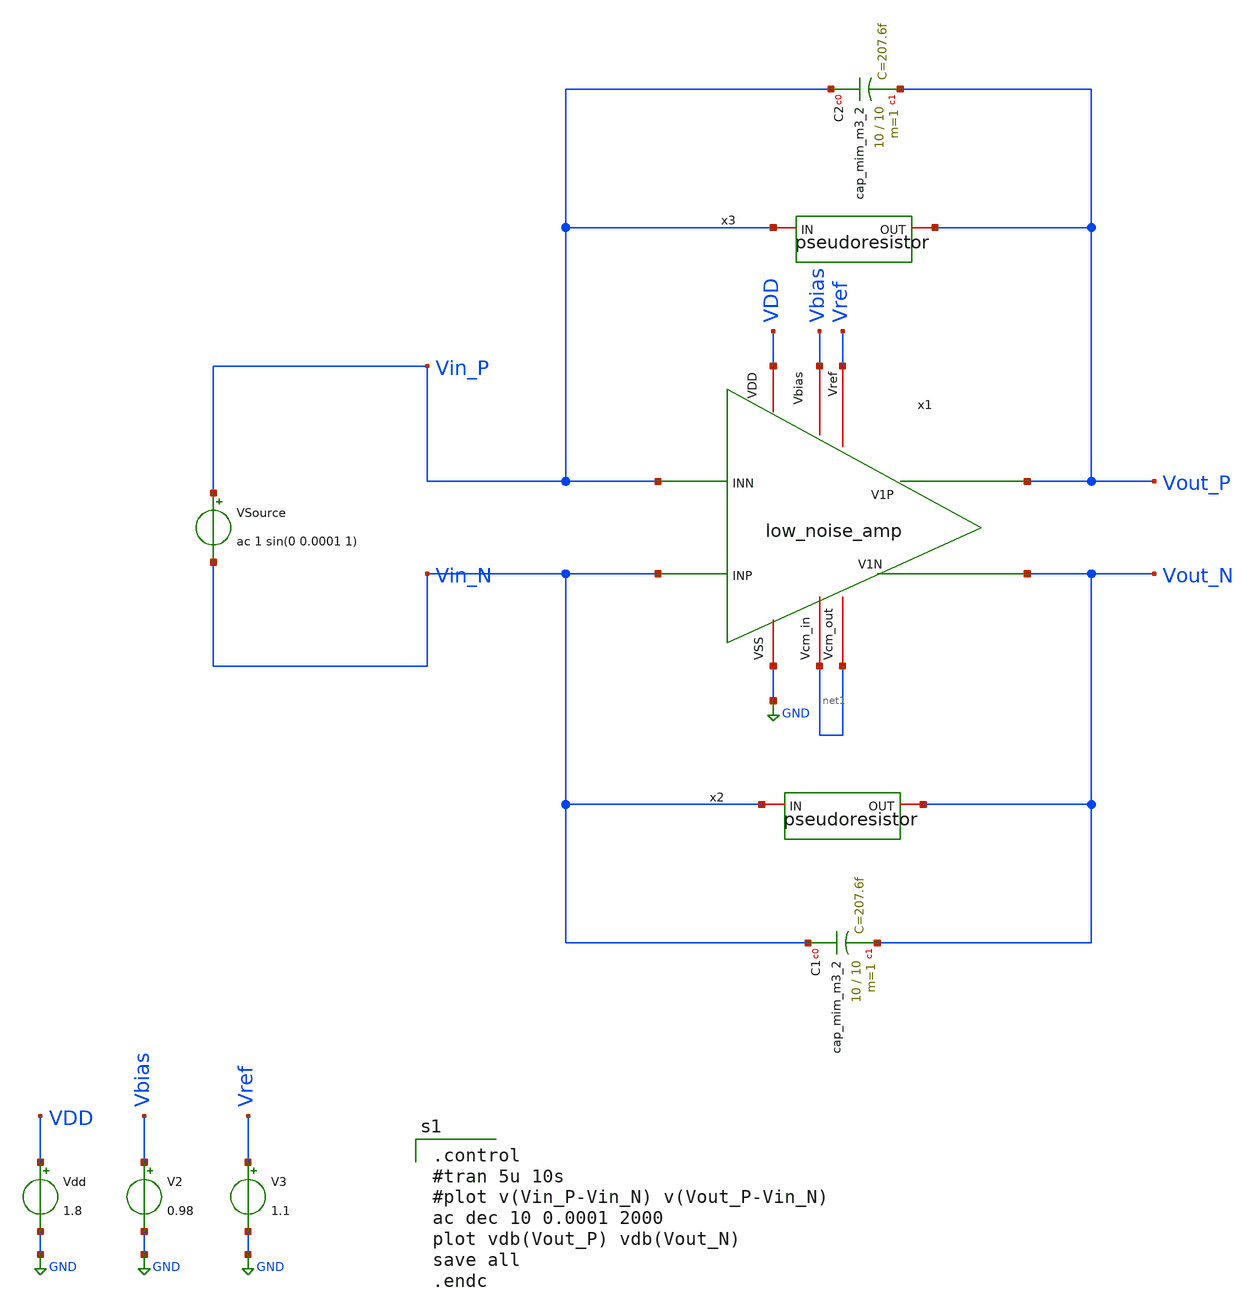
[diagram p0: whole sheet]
** sch_path: opamp_lna/low_noise_amp_tb.sch
**.subckt low_noise_amp_tb
x1 VDD net1 Vin_P Vin_N Vout_P Vout_N GND net1 Vbias Vref low_noise_amp
Vdd VDD GND 1.8
V2 Vbias GND 0.98
V3 Vref GND 1.1
VSource Vin_P Vin_N ac 1 sin(0 0.0001 1)
x2 Vin_N Vout_N pseudoresistor
x3 Vin_P Vout_P pseudoresistor
XC1 Vin_N Vout_N sky130_fd_pr__cap_mim_m3_2 W=10 L=10 MF=1 m=1
XC2 Vin_P Vout_P sky130_fd_pr__cap_mim_m3_2 W=10 L=10 MF=1 m=1
**** begin user architecture code

** opencircuitdesign pdks install
.lib $::SKYWATER_MODELS/sky130.lib.spice tt



.control
#tran 5u 10s
#plot v(Vin_P-Vin_N) v(Vout_P-Vin_N)
ac dec 10 0.0001 2000
plot vdb(Vout_P) vdb(Vout_N)
save all
.endc

**** end user architecture code
**.ends

* expanding   symbol:  low_noise_amp.sym # of pins=10
** sym_path: opamp_lna/low_noise_amp.sym
** sch_path: opamp_lna/low_noise_amp.sch
.subckt low_noise_amp VDD Vcm_in INN INP V1P V1N VSS Vcm_out Vbias Vref
*.iopin VDD
*.iopin VSS
*.iopin Vbias
*.ipin INP
*.ipin INN
*.iopin Vref
*.iopin Vcm_in
*.iopin Vcm_out
*.opin V1N
*.opin V1P
XM3 CMFB Vref net1 VDD sky130_fd_pr__pfet_01v8 L=0.8 W=4 nf=1 ad='int((nf+1)/2) * W/nf * 0.29' as='int((nf+2)/2) * W/nf * 0.29'
+ pd='2*int((nf+1)/2) * (W/nf + 0.29)' ps='2*int((nf+2)/2) * (W/nf + 0.29)' nrd='0.29 / W' nrs='0.29 / W'
+ sa=0 sb=0 sd=0 mult=1 m=1
XM11 net1 Vbias VDD VDD sky130_fd_pr__pfet_01v8 L=0.8 W=1 nf=1 ad='int((nf+1)/2) * W/nf * 0.29' as='int((nf+2)/2) * W/nf * 0.29'
+ pd='2*int((nf+1)/2) * (W/nf + 0.29)' ps='2*int((nf+2)/2) * (W/nf + 0.29)' nrd='0.29 / W' nrs='0.29 / W'
+ sa=0 sb=0 sd=0 mult=1 m=1
XM7 V1N INP B0 VDD sky130_fd_pr__pfet_01v8 L=2 W=16 nf=1 ad='int((nf+1)/2) * W/nf * 0.29' as='int((nf+2)/2) * W/nf * 0.29'
+ pd='2*int((nf+1)/2) * (W/nf + 0.29)' ps='2*int((nf+2)/2) * (W/nf + 0.29)' nrd='0.29 / W' nrs='0.29 / W'
+ sa=0 sb=0 sd=0 mult=1 m=1
XM8 V1P INN B0 VDD sky130_fd_pr__pfet_01v8 L=2 W=16 nf=1 ad='int((nf+1)/2) * W/nf * 0.29' as='int((nf+2)/2) * W/nf * 0.29'
+ pd='2*int((nf+1)/2) * (W/nf + 0.29)' ps='2*int((nf+2)/2) * (W/nf + 0.29)' nrd='0.29 / W' nrs='0.29 / W'
+ sa=0 sb=0 sd=0 mult=1 m=1
XM9 V1N INP net3 VSS sky130_fd_pr__nfet_01v8 L=1 W=8 nf=1 ad='int((nf+1)/2) * W/nf * 0.29' as='int((nf+2)/2) * W/nf * 0.29'
+ pd='2*int((nf+1)/2) * (W/nf + 0.29)' ps='2*int((nf+2)/2) * (W/nf + 0.29)' nrd='0.29 / W' nrs='0.29 / W'
+ sa=0 sb=0 sd=0 mult=1 m=1
XM12 B0 Vbias VDD VDD sky130_fd_pr__pfet_01v8 L=0.800 W=2 nf=1 ad='int((nf+1)/2) * W/nf * 0.29' as='int((nf+2)/2) * W/nf * 0.29'
+ pd='2*int((nf+1)/2) * (W/nf + 0.29)' ps='2*int((nf+2)/2) * (W/nf + 0.29)' nrd='0.29 / W' nrs='0.29 / W'
+ sa=0 sb=0 sd=0 mult=1 m=1
XM13 net3 CMFB VSS VSS sky130_fd_pr__nfet_01v8 L=0.8 W=2 nf=1 ad='int((nf+1)/2) * W/nf * 0.29' as='int((nf+2)/2) * W/nf * 0.29'
+ pd='2*int((nf+1)/2) * (W/nf + 0.29)' ps='2*int((nf+2)/2) * (W/nf + 0.29)' nrd='0.29 / W' nrs='0.29 / W'
+ sa=0 sb=0 sd=0 mult=1 m=1
XM15 Vcm_out Vcm_out net4 Vcm_out sky130_fd_pr__pfet_01v8 L=0.15 W=1 nf=1 ad='int((nf+1)/2) * W/nf * 0.29'
+ as='int((nf+2)/2) * W/nf * 0.29' pd='2*int((nf+1)/2) * (W/nf + 0.29)' ps='2*int((nf+2)/2) * (W/nf + 0.29)'
+ nrd='0.29 / W' nrs='0.29 / W' sa=0 sb=0 sd=0 mult=1 m=1
XM16 net4 V1P V1P V1P sky130_fd_pr__pfet_01v8 L=0.15 W=1 nf=1 ad='int((nf+1)/2) * W/nf * 0.29' as='int((nf+2)/2) * W/nf * 0.29'
+ pd='2*int((nf+1)/2) * (W/nf + 0.29)' ps='2*int((nf+2)/2) * (W/nf + 0.29)' nrd='0.29 / W' nrs='0.29 / W'
+ sa=0 sb=0 sd=0 mult=1 m=1
XM17 Vcm_out Vcm_out net5 Vcm_out sky130_fd_pr__pfet_01v8 L=0.15 W=1 nf=1 ad='int((nf+1)/2) * W/nf * 0.29'
+ as='int((nf+2)/2) * W/nf * 0.29' pd='2*int((nf+1)/2) * (W/nf + 0.29)' ps='2*int((nf+2)/2) * (W/nf + 0.29)'
+ nrd='0.29 / W' nrs='0.29 / W' sa=0 sb=0 sd=0 mult=1 m=1
XM18 net5 V1N V1N V1N sky130_fd_pr__pfet_01v8 L=0.15 W=1 nf=1 ad='int((nf+1)/2) * W/nf * 0.29' as='int((nf+2)/2) * W/nf * 0.29'
+ pd='2*int((nf+1)/2) * (W/nf + 0.29)' ps='2*int((nf+2)/2) * (W/nf + 0.29)' nrd='0.29 / W' nrs='0.29 / W'
+ sa=0 sb=0 sd=0 mult=1 m=1
XC1 Vcm_out VSS sky130_fd_pr__cap_mim_m3_1 W=1 L=1 MF=1 m=1
XM1 V1P INN net3 VSS sky130_fd_pr__nfet_01v8 L=1 W=8 nf=1 ad='int((nf+1)/2) * W/nf * 0.29' as='int((nf+2)/2) * W/nf * 0.29'
+ pd='2*int((nf+1)/2) * (W/nf + 0.29)' ps='2*int((nf+2)/2) * (W/nf + 0.29)' nrd='0.29 / W' nrs='0.29 / W'
+ sa=0 sb=0 sd=0 mult=1 m=1
XM2 net2 net2 VSS VSS sky130_fd_pr__nfet_01v8 L=0.8 W=2 nf=1 ad='int((nf+1)/2) * W/nf * 0.29' as='int((nf+2)/2) * W/nf * 0.29'
+ pd='2*int((nf+1)/2) * (W/nf + 0.29)' ps='2*int((nf+2)/2) * (W/nf + 0.29)' nrd='0.29 / W' nrs='0.29 / W'
+ sa=0 sb=0 sd=0 mult=1 m=1
XM5 CMFB net2 VSS VSS sky130_fd_pr__nfet_01v8 L=0.8 W=2 nf=1 ad='int((nf+1)/2) * W/nf * 0.29' as='int((nf+2)/2) * W/nf * 0.29'
+ pd='2*int((nf+1)/2) * (W/nf + 0.29)' ps='2*int((nf+2)/2) * (W/nf + 0.29)' nrd='0.29 / W' nrs='0.29 / W'
+ sa=0 sb=0 sd=0 mult=1 m=1
XM6 net2 Vcm_in net1 VDD sky130_fd_pr__pfet_01v8 L=0.8 W=4 nf=1 ad='int((nf+1)/2) * W/nf * 0.29' as='int((nf+2)/2) * W/nf * 0.29'
+ pd='2*int((nf+1)/2) * (W/nf + 0.29)' ps='2*int((nf+2)/2) * (W/nf + 0.29)' nrd='0.29 / W' nrs='0.29 / W'
+ sa=0 sb=0 sd=0 mult=1 m=1
.ends


* expanding   symbol:  /home/lcg3895/CE393/pseudoresistor.sym # of pins=2
** sym_path: opamp_lna/pseudoresistor.sym
** sch_path: opamp_lna/pseudoresistor.sch
.subckt pseudoresistor IN OUT
*.iopin IN
*.iopin OUT
XM5 net1 IN IN IN sky130_fd_pr__pfet_01v8 L=0.5 W=1 nf=1 ad='int((nf+1)/2) * W/nf * 0.29' as='int((nf+2)/2) * W/nf * 0.29'
+ pd='2*int((nf+1)/2) * (W/nf + 0.29)' ps='2*int((nf+2)/2) * (W/nf + 0.29)' nrd='0.29 / W' nrs='0.29 / W'
+ sa=0 sb=0 sd=0 mult=10 m=10
XM1 net2 net2 net1 net2 sky130_fd_pr__pfet_01v8 L=0.5 W=1 nf=1 ad='int((nf+1)/2) * W/nf * 0.29' as='int((nf+2)/2) * W/nf * 0.29'
+ pd='2*int((nf+1)/2) * (W/nf + 0.29)' ps='2*int((nf+2)/2) * (W/nf + 0.29)' nrd='0.29 / W' nrs='0.29 / W'
+ sa=0 sb=0 sd=0 mult=10 m=10
XM2 net3 net2 net2 net2 sky130_fd_pr__pfet_01v8 L=0.5 W=1 nf=1 ad='int((nf+1)/2) * W/nf * 0.29' as='int((nf+2)/2) * W/nf * 0.29'
+ pd='2*int((nf+1)/2) * (W/nf + 0.29)' ps='2*int((nf+2)/2) * (W/nf + 0.29)' nrd='0.29 / W' nrs='0.29 / W'
+ sa=0 sb=0 sd=0 mult=10 m=10
XM3 OUT OUT net3 OUT sky130_fd_pr__pfet_01v8 L=0.5 W=1.2 nf=1 ad='int((nf+1)/2) * W/nf * 0.29' as='int((nf+2)/2) * W/nf * 0.29'
+ pd='2*int((nf+1)/2) * (W/nf + 0.29)' ps='2*int((nf+2)/2) * (W/nf + 0.29)' nrd='0.29 / W' nrs='0.29 / W'
+ sa=0 sb=0 sd=0 mult=1 m=1
.ends

.GLOBAL GND
.end
